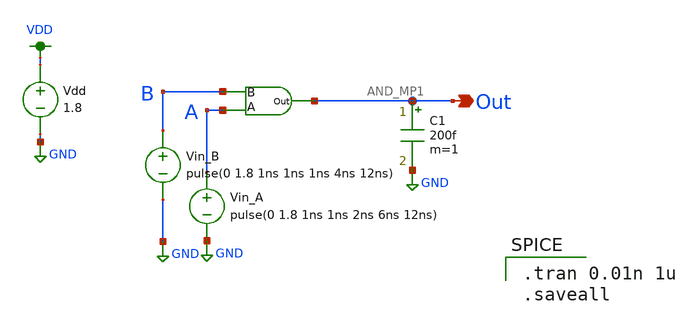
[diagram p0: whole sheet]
** sch_path: MP1/MP1_final_schem.sch
**.subckt MP1_final_schem Out
*.opin Out
x1 B Out A AND_MP1
C1 Out GND 200f m=1
Vin_B B GND pulse(0 1.8 1ns 1ns 1ns 4ns 12ns)
Vin_A A GND pulse(0 1.8 1ns 1ns 2ns 6ns 12ns)
Vdd VDD GND 1.8
**** begin user architecture code

.option wnflag=1
.lib ~/skywater/skywater-pdk/libraries/sky130_fd_pr_ngspice/latest/models/sky130.lib.spice tt


.tran 0.01n 1u
.saveall

**** end user architecture code
**.ends

* expanding   symbol:  /home/madvlsi/Documents/MP1/AND_MP1.sym # of pins=3
** sym_path: MP1/AND_MP1.sym
** sch_path: MP1/AND_MP1.sch
.subckt AND_MP1 B Out A
*.ipin B
*.ipin A
*.opin Out
x1 B A net1 NAND_mp1
x2 Out net1 INV_mp1
.ends


* expanding   symbol:  /home/madvlsi/Documents/MP1/NAND_mp1.sym # of pins=3
** sym_path: MP1/NAND_mp1.sym
** sch_path: MP1/NAND_mp1.sch
.subckt NAND_mp1 B A out
*.ipin A
*.ipin B
*.opin out
XM1 out A VDD VDD sky130_fd_pr__pfet_01v8 L=0.15 W=1 nf=1 ad='int((nf+1)/2) * W/nf * 0.29' as='int((nf+2)/2) * W/nf * 0.29'
+ pd='2*int((nf+1)/2) * (W/nf + 0.29)' ps='2*int((nf+2)/2) * (W/nf + 0.29)' nrd='0.29 / W' nrs='0.29 / W'
+ sa=0 sb=0 sd=0 mult=1 m=1
XM2 out B VDD VDD sky130_fd_pr__pfet_01v8 L=0.15 W=1 nf=1 ad='int((nf+1)/2) * W/nf * 0.29' as='int((nf+2)/2) * W/nf * 0.29'
+ pd='2*int((nf+1)/2) * (W/nf + 0.29)' ps='2*int((nf+2)/2) * (W/nf + 0.29)' nrd='0.29 / W' nrs='0.29 / W'
+ sa=0 sb=0 sd=0 mult=1 m=1
XM3 out A net1 GND sky130_fd_pr__nfet_01v8 L=0.15 W=1 nf=1 ad='int((nf+1)/2) * W/nf * 0.29' as='int((nf+2)/2) * W/nf * 0.29'
+ pd='2*int((nf+1)/2) * (W/nf + 0.29)' ps='2*int((nf+2)/2) * (W/nf + 0.29)' nrd='0.29 / W' nrs='0.29 / W'
+ sa=0 sb=0 sd=0 mult=1 m=1
XM5 net1 B GND GND sky130_fd_pr__nfet_01v8 L=0.15 W=1 nf=1 ad='int((nf+1)/2) * W/nf * 0.29' as='int((nf+2)/2) * W/nf * 0.29'
+ pd='2*int((nf+1)/2) * (W/nf + 0.29)' ps='2*int((nf+2)/2) * (W/nf + 0.29)' nrd='0.29 / W' nrs='0.29 / W'
+ sa=0 sb=0 sd=0 mult=1 m=1
.ends


* expanding   symbol:  /home/madvlsi/Documents/MP1/INV_mp1.sym # of pins=2
** sym_path: MP1/INV_mp1.sym
** sch_path: MP1/INV_mp1.sch
.subckt INV_mp1 out A
*.ipin A
*.opin out
XM1 out A VDD VDD sky130_fd_pr__pfet_01v8 L=0.15 W=1 nf=1 ad='int((nf+1)/2) * W/nf * 0.29' as='int((nf+2)/2) * W/nf * 0.29'
+ pd='2*int((nf+1)/2) * (W/nf + 0.29)' ps='2*int((nf+2)/2) * (W/nf + 0.29)' nrd='0.29 / W' nrs='0.29 / W'
+ sa=0 sb=0 sd=0 mult=1 m=1
XM2 out A GND GND sky130_fd_pr__nfet_01v8 L=0.15 W=1 nf=1 ad='int((nf+1)/2) * W/nf * 0.29' as='int((nf+2)/2) * W/nf * 0.29'
+ pd='2*int((nf+1)/2) * (W/nf + 0.29)' ps='2*int((nf+2)/2) * (W/nf + 0.29)' nrd='0.29 / W' nrs='0.29 / W'
+ sa=0 sb=0 sd=0 mult=1 m=1
.ends

.GLOBAL GND
.GLOBAL VDD
.end
